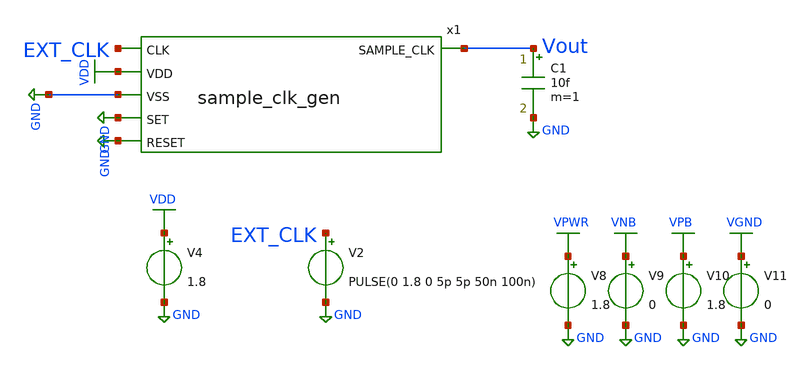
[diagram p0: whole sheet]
** sch_path: module/top_comp_sar/top_comp_sar_parasitic/tb_sample_clk_gen.sch
**.subckt tb_sample_clk_gen
V2 EXT_CLK GND PULSE(0 1.8 0 5p 5p 50n 100n)
V4 VDD GND 1.8
x1 Vout EXT_CLK VDD GND GND GND sample_clk_gen
C1 Vout GND 10f m=1
V8 VPWR GND 1.8
V9 VNB GND 0
V10 VPB GND 1.8
V11 VGND GND 0
**** begin user architecture code



.lib /foss/pdks/sky130A/libs.tech/ngspice/sky130.lib.spice ff
.include /foss/pdks/sky130A/libs.ref/sky130_fd_sc_hd/spice/sky130_fd_sc_hd.spice


.tran 10ps 400ns

.control
	option temp = 0
	let vdd_act = 1.98

	alter V1 vdd_act

	run
	plot V(Vout) V(EXT_CLK)

	let l_vdd = vdd_act * 0.2
        let h_vdd = vdd_act * 0.8
        let m_vdd = vdd_act * 0.5
        meas tran rising_s find time when V(Vout)=l_vdd RISE=1 TD=90n
        meas tran rising_e find time when V(Vout)=h_vdd RISE=1 TD=90n
        let rising_time = rising_e-rising_s
        meas tran falling_s find time when V(Vout)=h_vdd FALL=1 TD=90n
        meas tran falling_e find time when V(Vout)=l_vdd FALL=1 TD=90n
        let falling_time = falling_e-falling_s
        meas tran IN find time when V(ext_clk)=m_vdd RISE=1 TD=90n
        meas tran OUT find time when V(Vout)=m_vdd RISE=1 TD=90n
        let rising_delay = OUT-IN

	meas tran IN find time when V(Vout)=m_vdd RISE=1 TD=90n
        meas tran OUT find time when V(Vout)=m_vdd FALL=1 TD=90n
        let on_time = OUT-IN

	print rising_time falling_time rising_delay on_time
.endc
.save all



**** end user architecture code
**.ends
.GLOBAL GND
.GLOBAL VDD
.GLOBAL VGND
.GLOBAL VNB
.GLOBAL VPB
.GLOBAL VPWR
.end
